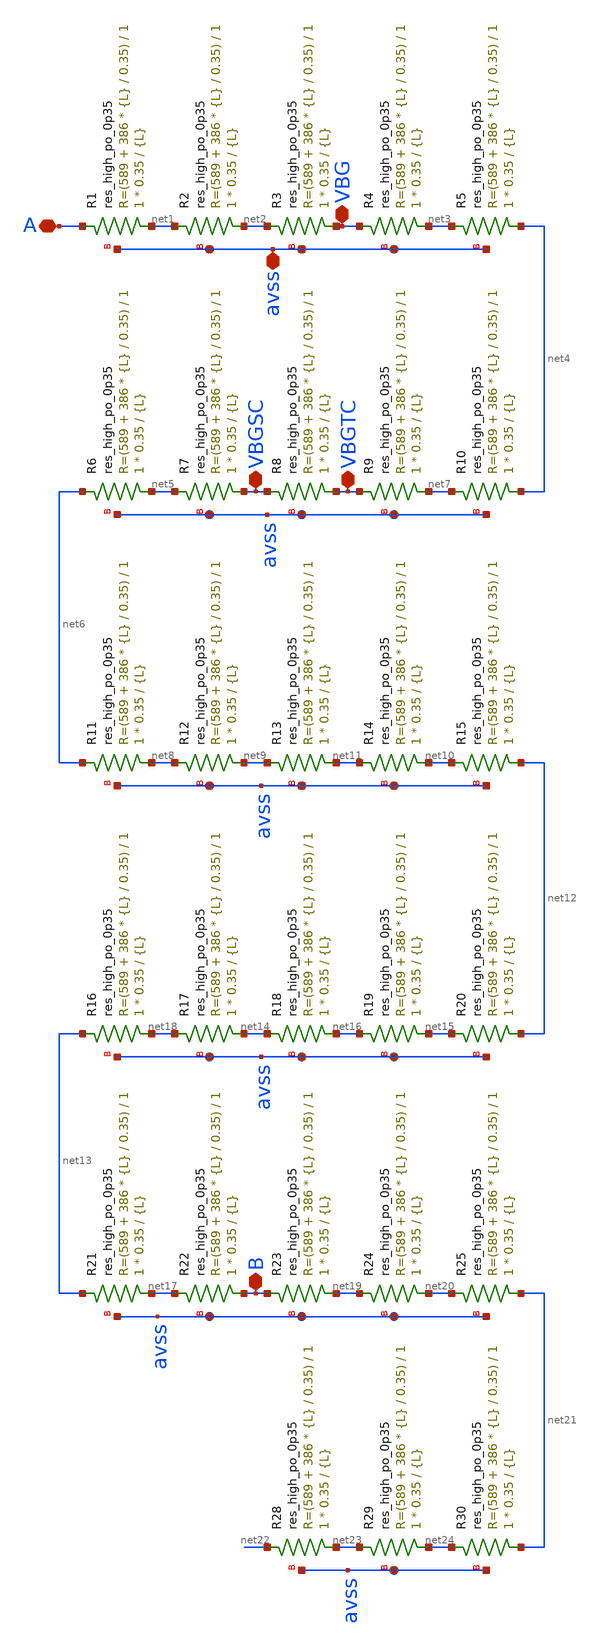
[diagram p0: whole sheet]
** sch_path: xschem/Resistor492k_1.sch
**.subckt Resistor492k_1 A VBGTC B VBGSC VBG avss
*.iopin A
*.iopin VBGTC
*.iopin B
*.iopin VBGSC
*.iopin VBG
*.iopin avss
XR1 net1 A avss sky130_fd_pr__res_high_po_0p35 L={L} mult=1 m=1
XR2 net2 net1 avss sky130_fd_pr__res_high_po_0p35 L={L} mult=1 m=1
XR3 VBG net2 avss sky130_fd_pr__res_high_po_0p35 L={L} mult=1 m=1
XR4 net3 VBG avss sky130_fd_pr__res_high_po_0p35 L={L} mult=1 m=1
XR5 net4 net3 avss sky130_fd_pr__res_high_po_0p35 L={L} mult=1 m=1
XR6 net5 net6 avss sky130_fd_pr__res_high_po_0p35 L={L} mult=1 m=1
XR7 VBGSC net5 avss sky130_fd_pr__res_high_po_0p35 L={L} mult=1 m=1
XR8 VBGTC VBGSC avss sky130_fd_pr__res_high_po_0p35 L={L} mult=1 m=1
XR9 net7 VBGTC avss sky130_fd_pr__res_high_po_0p35 L={L} mult=1 m=1
XR10 net4 net7 avss sky130_fd_pr__res_high_po_0p35 L={L} mult=1 m=1
XR11 net8 net6 avss sky130_fd_pr__res_high_po_0p35 L={L} mult=1 m=1
XR12 net9 net8 avss sky130_fd_pr__res_high_po_0p35 L={L} mult=1 m=1
XR13 net11 net9 avss sky130_fd_pr__res_high_po_0p35 L={L} mult=1 m=1
XR14 net10 net11 avss sky130_fd_pr__res_high_po_0p35 L={L} mult=1 m=1
XR15 net12 net10 avss sky130_fd_pr__res_high_po_0p35 L={L} mult=1 m=1
XR16 net18 net13 avss sky130_fd_pr__res_high_po_0p35 L={L} mult=1 m=1
XR17 net14 net18 avss sky130_fd_pr__res_high_po_0p35 L={L} mult=1 m=1
XR18 net16 net14 avss sky130_fd_pr__res_high_po_0p35 L={L} mult=1 m=1
XR19 net15 net16 avss sky130_fd_pr__res_high_po_0p35 L={L} mult=1 m=1
XR20 net12 net15 avss sky130_fd_pr__res_high_po_0p35 L={L} mult=1 m=1
XR21 net17 net13 avss sky130_fd_pr__res_high_po_0p35 L={L} mult=1 m=1
XR22 B net17 avss sky130_fd_pr__res_high_po_0p35 L={L} mult=1 m=1
XR23 net19 B avss sky130_fd_pr__res_high_po_0p35 L={L} mult=1 m=1
XR24 net20 net19 avss sky130_fd_pr__res_high_po_0p35 L={L} mult=1 m=1
XR25 net21 net20 avss sky130_fd_pr__res_high_po_0p35 L={L} mult=1 m=1
XR28 net23 net22 avss sky130_fd_pr__res_high_po_0p35 L={L} mult=1 m=1
XR29 net24 net23 avss sky130_fd_pr__res_high_po_0p35 L={L} mult=1 m=1
XR30 net21 net24 avss sky130_fd_pr__res_high_po_0p35 L={L} mult=1 m=1
**** begin user architecture code


.param L=17


**** end user architecture code
**.ends
.end
